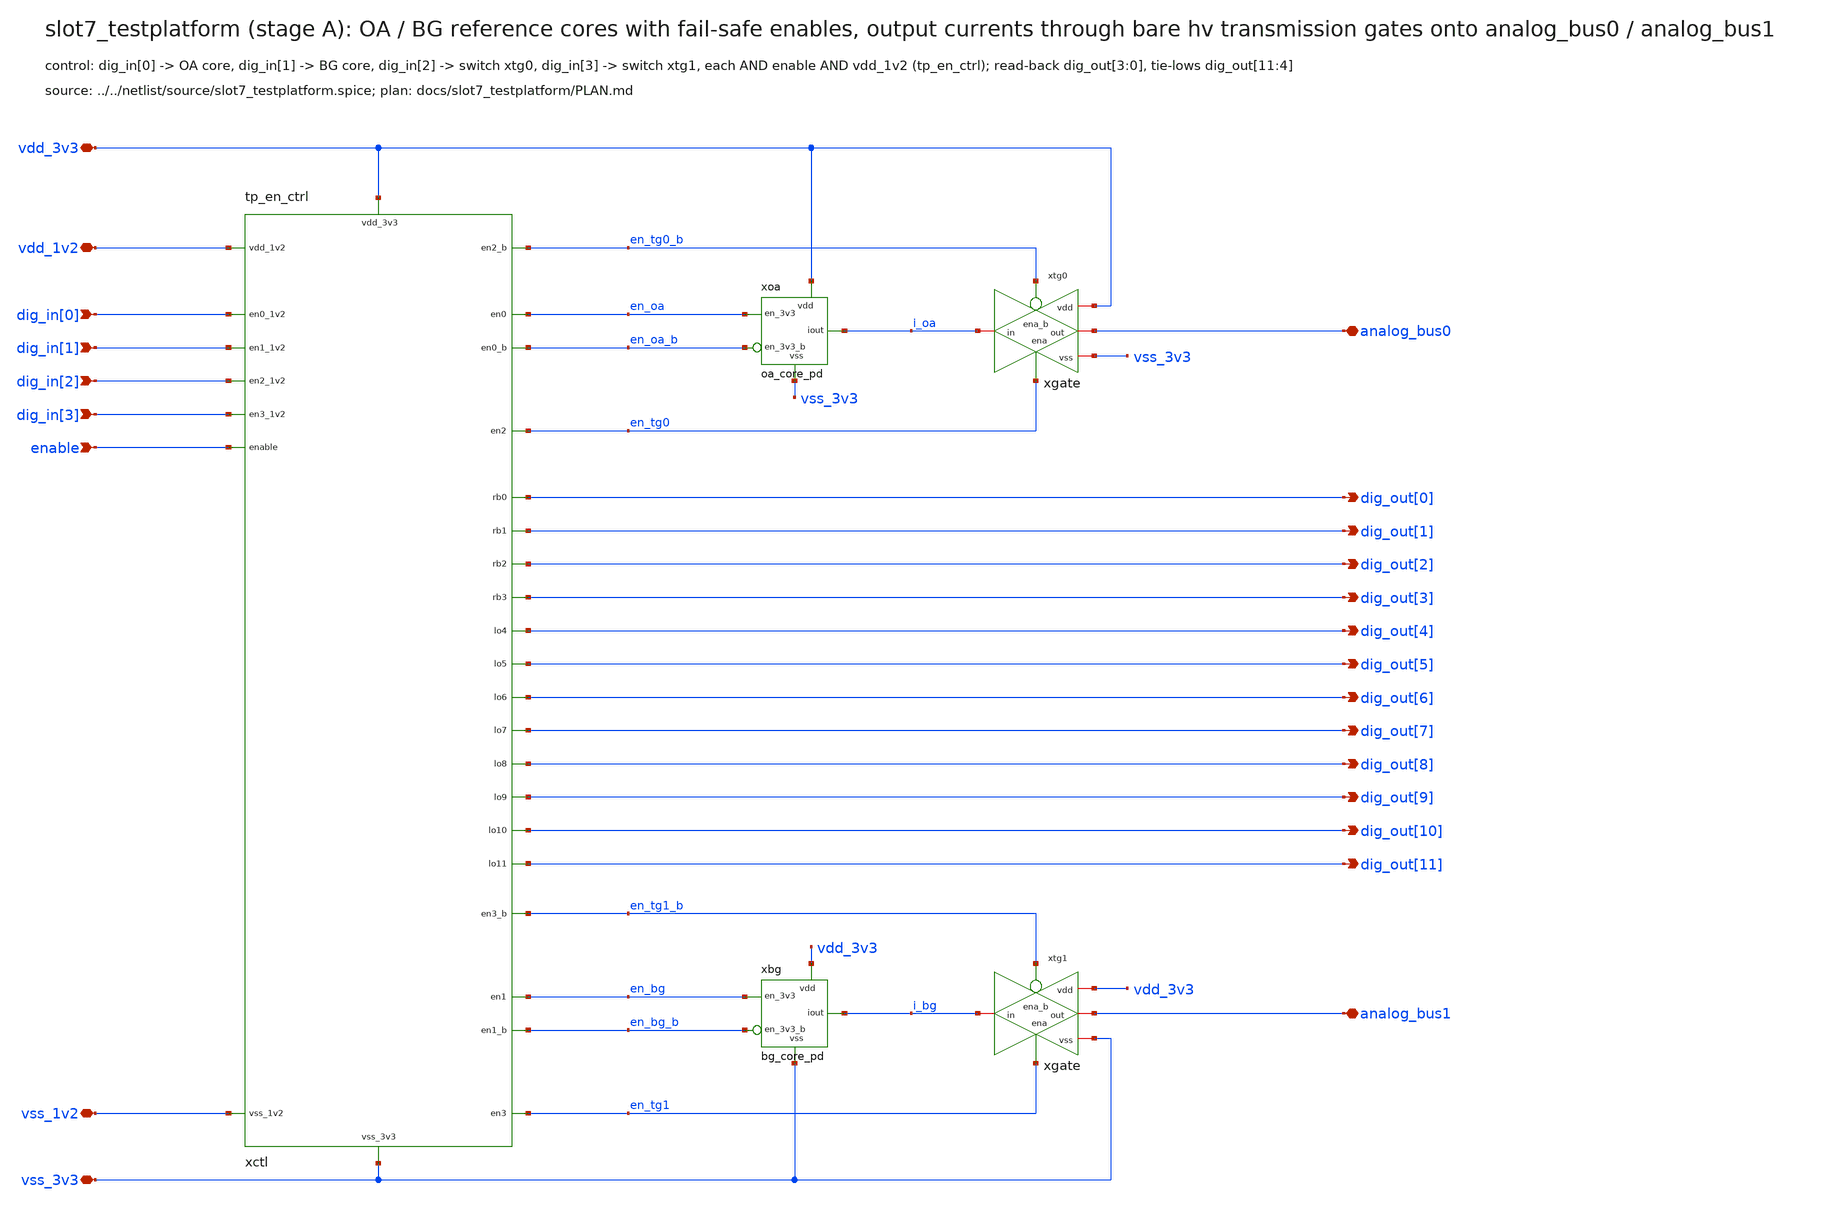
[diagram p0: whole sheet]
** sch_path: macros/slot7_testplatform/schematic/xschem_drawn/slot7_testplatform.sch
**.subckt slot7_testplatform vdd_3v3 vss_3v3 vdd_1v2 vss_1v2 enable dig_in[0] dig_in[1] dig_in[2]
*+ dig_in[3] dig_out[0] dig_out[1] dig_out[2] dig_out[3] dig_out[4] dig_out[5] dig_out[6] dig_out[7] dig_out[8]
*+ dig_out[9] dig_out[10] dig_out[11] analog_bus0 analog_bus1
*.iopin vdd_3v3
*.iopin vss_3v3
*.iopin vdd_1v2
*.iopin vss_1v2
*.ipin enable
*.ipin dig_in[0]
*.ipin dig_in[1]
*.ipin dig_in[2]
*.ipin dig_in[3]
*.opin dig_out[0]
*.opin dig_out[1]
*.opin dig_out[2]
*.opin dig_out[3]
*.opin dig_out[4]
*.opin dig_out[5]
*.opin dig_out[6]
*.opin dig_out[7]
*.opin dig_out[8]
*.opin dig_out[9]
*.opin dig_out[10]
*.opin dig_out[11]
*.iopin analog_bus0
*.iopin analog_bus1
xctl vdd_3v3 vss_3v3 vdd_1v2 vss_1v2 dig_in[0] dig_in[1] dig_in[2] dig_in[3] enable en_oa en_oa_b
+ en_bg en_bg_b en_tg0 en_tg0_b en_tg1 en_tg1_b dig_out[0] dig_out[1] dig_out[2] dig_out[3] dig_out[4]
+ dig_out[5] dig_out[6] dig_out[7] dig_out[8] dig_out[9] dig_out[10] dig_out[11] tp_en_ctrl
xoa vdd_3v3 vss_3v3 i_oa en_oa en_oa_b oa_core_pd
xtg0 en_tg0_b vdd_3v3 i_oa analog_bus0 vss_3v3 en_tg0 xgate
xbg vdd_3v3 vss_3v3 i_bg en_bg en_bg_b bg_core_pd
xtg1 en_tg1_b vdd_3v3 i_bg analog_bus1 vss_3v3 en_tg1 xgate
**.ends
.end
